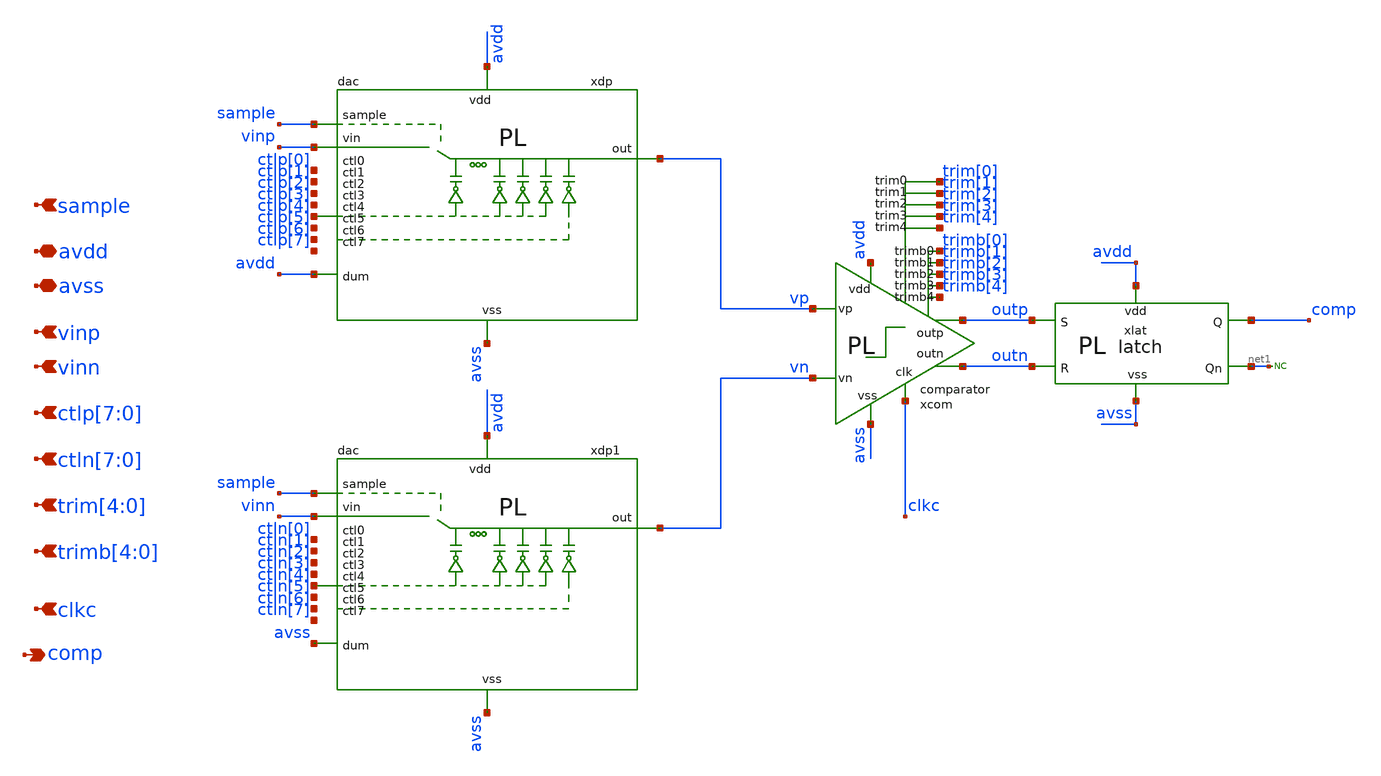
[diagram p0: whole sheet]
** sch_path: new_layout/simulations/symbols/sar_analog.sch
**.subckt sar_analog avss avdd vinp vinn sample
*+ ctlp[7],ctlp[6],ctlp[5],ctlp[4],ctlp[3],ctlp[2],ctlp[1],ctlp[0] ctln[7],ctln[6],ctln[5],ctln[4],ctln[3],ctln[2],ctln[1],ctln[0]
*+ trim[4],trim[3],trim[2],trim[1],trim[0] trimb[4],trimb[3],trimb[2],trimb[1],trimb[0] clkc comp
*.iopin avss
*.iopin avdd
*.ipin vinp
*.ipin vinn
*.ipin sample
*.ipin ctlp[7],ctlp[6],ctlp[5],ctlp[4],ctlp[3],ctlp[2],ctlp[1],ctlp[0]
*.ipin ctln[7],ctln[6],ctln[5],ctln[4],ctln[3],ctln[2],ctln[1],ctln[0]
*.ipin trim[4],trim[3],trim[2],trim[1],trim[0]
*.ipin trimb[4],trimb[3],trimb[2],trimb[1],trimb[0]
*.ipin clkc
*.opin comp
xlat avdd avss net1 outp outn comp latch
* noconn #net1
xdp sample vinp ctlp[0] ctlp[1] ctlp[3] ctlp[2] ctlp[4] ctlp[5] ctlp[6] ctlp[7] avdd avss vp avdd
+ dac
xcom trim[4] trim[3] trim[2] trim[1] vp vn outp outn clkc avdd trimb[1] trimb[2] trimb[3] trimb[4]
+ trimb[0] trim[0] avss comparator
xdp1 sample vinn ctln[0] ctln[1] ctln[3] ctln[2] ctln[4] ctln[5] ctln[6] ctln[7] avss avss vn avdd
+ dac
**.ends
.end
